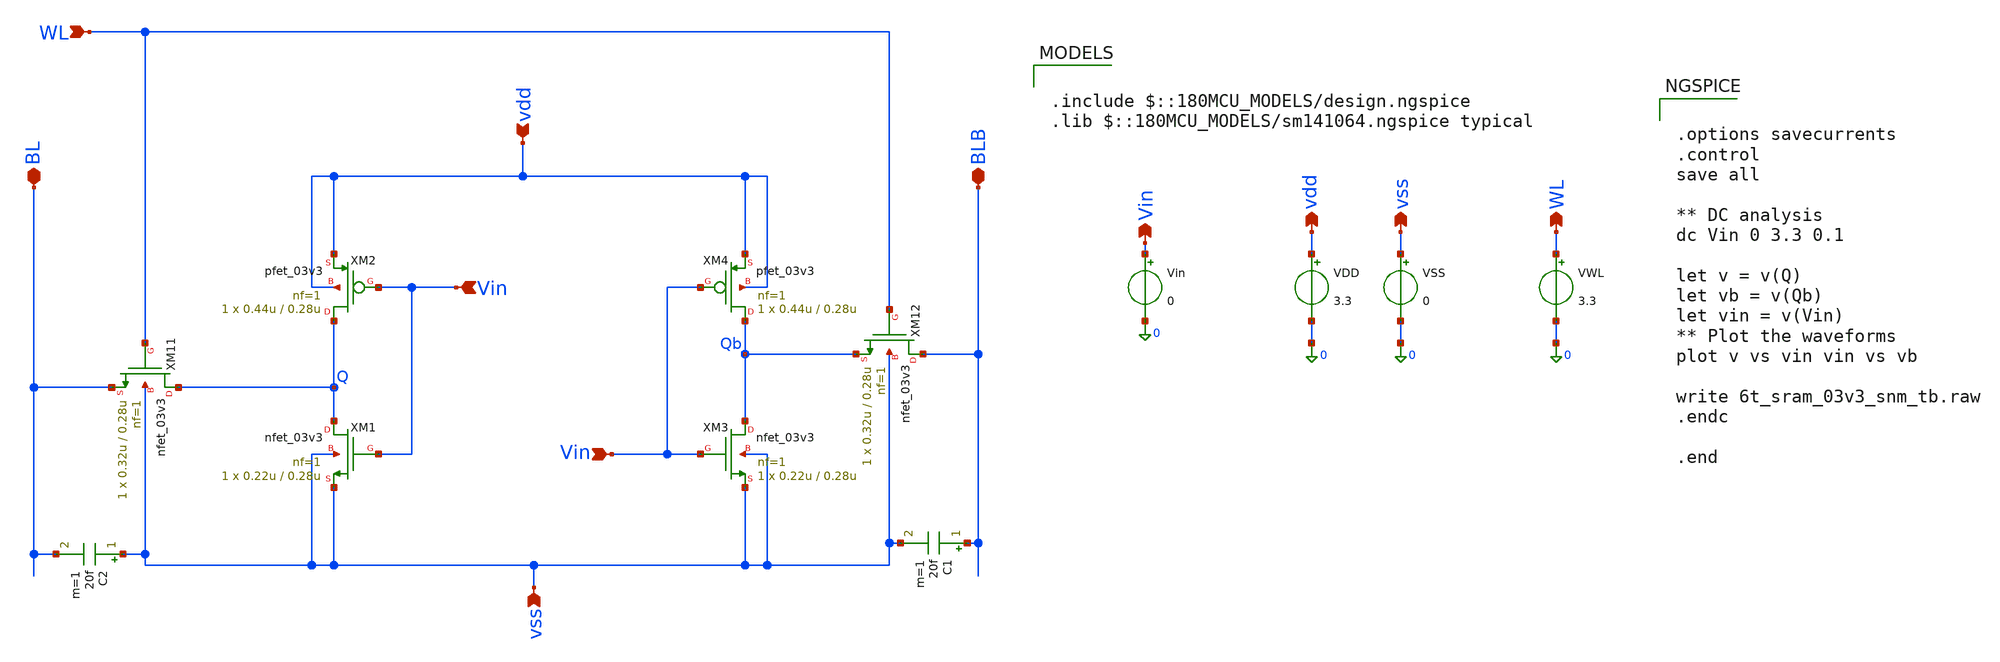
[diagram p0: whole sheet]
** sch_path: analog/tests/6t_sram_03v3_read_snm_tb.sch
**.subckt 6t_sram_03v3_read_snm_tb vdd vss vdd vss Vin Vin BL WL BLB WL Vin
*.ipin vdd
*.ipin vss
*.opin vdd
*.opin vss
*.opin Vin
*.ipin Vin
*.iopin BL
*.ipin WL
*.iopin BLB
*.opin WL
*.ipin Vin
XM1 Q Vin vss vss nfet_03v3 L=0.28u W=0.22u nf=1 ad='int((nf+1)/2) * W/nf * 0.18u' as='int((nf+2)/2) * W/nf * 0.18u'
+ pd='2*int((nf+1)/2) * (W/nf + 0.18u)' ps='2*int((nf+2)/2) * (W/nf + 0.18u)' nrd='0.18u / W' nrs='0.18u / W'
+ sa=0 sb=0 sd=0 m=1
XM2 Q Vin vdd vdd pfet_03v3 L=0.28u W=0.44u nf=1 ad='int((nf+1)/2) * W/nf * 0.18u' as='int((nf+2)/2) * W/nf * 0.18u'
+ pd='2*int((nf+1)/2) * (W/nf + 0.18u)' ps='2*int((nf+2)/2) * (W/nf + 0.18u)' nrd='0.18u / W' nrs='0.18u / W'
+ sa=0 sb=0 sd=0 m=1
XM3 Qb Vin vss vss nfet_03v3 L=0.28u W=0.22u nf=1 ad='int((nf+1)/2) * W/nf * 0.18u' as='int((nf+2)/2) * W/nf * 0.18u'
+ pd='2*int((nf+1)/2) * (W/nf + 0.18u)' ps='2*int((nf+2)/2) * (W/nf + 0.18u)' nrd='0.18u / W' nrs='0.18u / W'
+ sa=0 sb=0 sd=0 m=1
XM4 Qb Vin vdd vdd pfet_03v3 L=0.28u W=0.44u nf=1 ad='int((nf+1)/2) * W/nf * 0.18u' as='int((nf+2)/2) * W/nf * 0.18u'
+ pd='2*int((nf+1)/2) * (W/nf + 0.18u)' ps='2*int((nf+2)/2) * (W/nf + 0.18u)' nrd='0.18u / W' nrs='0.18u / W'
+ sa=0 sb=0 sd=0 m=1
VDD vdd 0 3.3
VSS vss 0 0
Vin Vin 0 0
XM11 Q WL BL vss nfet_03v3 L=0.28u W=0.32u nf=1 ad='int((nf+1)/2) * W/nf * 0.18u' as='int((nf+2)/2) * W/nf * 0.18u'
+ pd='2*int((nf+1)/2) * (W/nf + 0.18u)' ps='2*int((nf+2)/2) * (W/nf + 0.18u)' nrd='0.18u / W' nrs='0.18u / W'
+ sa=0 sb=0 sd=0 m=1
XM12 BLB WL Qb vss nfet_03v3 L=0.28u W=0.32u nf=1 ad='int((nf+1)/2) * W/nf * 0.18u' as='int((nf+2)/2) * W/nf * 0.18u'
+ pd='2*int((nf+1)/2) * (W/nf + 0.18u)' ps='2*int((nf+2)/2) * (W/nf + 0.18u)' nrd='0.18u / W' nrs='0.18u / W'
+ sa=0 sb=0 sd=0 m=1
VWL WL 0 3.3
C1 BLB vss 20f m=1
C2 vss BL 20f m=1
**** begin user architecture code

.include $::180MCU_MODELS/design.ngspice
.lib $::180MCU_MODELS/sm141064.ngspice typical



.options savecurrents
.control
save all

** DC analysis
dc Vin 0 3.3 0.1

let v = v(Q)
let vb = v(Qb)
let vin = v(Vin)
** Plot the waveforms
plot v vs vin vin vs vb

write 6t_sram_03v3_snm_tb.raw
.endc

.end


**** end user architecture code
**.ends
.end
